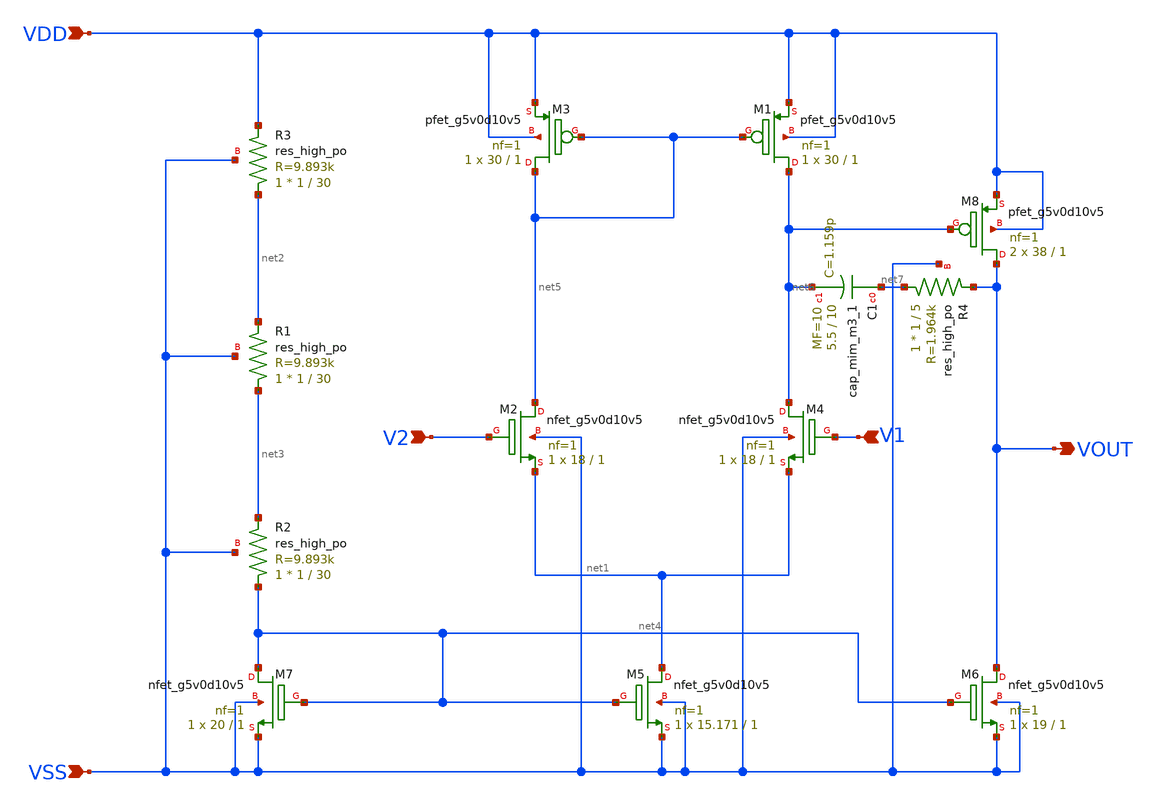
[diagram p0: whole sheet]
** sch_path: xschem/opamp.sch
**.subckt opamp VSS VDD V2 V1 VOUT
*.ipin VSS
*.ipin VDD
*.ipin V2
*.ipin V1
*.opin VOUT
XM2 net5 V2 net1 VSS sky130_fd_pr__nfet_g5v0d10v5 L=1 W=18 nf=1 ad='int((nf+1)/2) * W/nf * 0.29' as='int((nf+2)/2) * W/nf * 0.29'
+ pd='2*int((nf+1)/2) * (W/nf + 0.29)' ps='2*int((nf+2)/2) * (W/nf + 0.29)' nrd='0.29 / W' nrs='0.29 / W'
+ sa=0 sb=0 sd=0 mult=1 m=1
XM1 net6 net5 VDD VDD sky130_fd_pr__pfet_g5v0d10v5 L=1 W=30 nf=1 ad='int((nf+1)/2) * W/nf * 0.29' as='int((nf+2)/2) * W/nf * 0.29'
+ pd='2*int((nf+1)/2) * (W/nf + 0.29)' ps='2*int((nf+2)/2) * (W/nf + 0.29)' nrd='0.29 / W' nrs='0.29 / W'
+ sa=0 sb=0 sd=0 mult=1 m=1
XM4 net6 V1 net1 VSS sky130_fd_pr__nfet_g5v0d10v5 L=1 W=18 nf=1 ad='int((nf+1)/2) * W/nf * 0.29' as='int((nf+2)/2) * W/nf * 0.29'
+ pd='2*int((nf+1)/2) * (W/nf + 0.29)' ps='2*int((nf+2)/2) * (W/nf + 0.29)' nrd='0.29 / W' nrs='0.29 / W'
+ sa=0 sb=0 sd=0 mult=1 m=1
XM5 net1 net4 VSS VSS sky130_fd_pr__nfet_g5v0d10v5 L=1 W=15.171 nf=1 ad='int((nf+1)/2) * W/nf * 0.29'
+ as='int((nf+2)/2) * W/nf * 0.29' pd='2*int((nf+1)/2) * (W/nf + 0.29)' ps='2*int((nf+2)/2) * (W/nf + 0.29)'
+ nrd='0.29 / W' nrs='0.29 / W' sa=0 sb=0 sd=0 mult=1 m=1
XM6 VOUT net4 VSS VSS sky130_fd_pr__nfet_g5v0d10v5 L=1 W=19 nf=1 ad='int((nf+1)/2) * W/nf * 0.29' as='int((nf+2)/2) * W/nf * 0.29'
+ pd='2*int((nf+1)/2) * (W/nf + 0.29)' ps='2*int((nf+2)/2) * (W/nf + 0.29)' nrd='0.29 / W' nrs='0.29 / W'
+ sa=0 sb=0 sd=0 mult=1 m=1
XM7 net4 net4 VSS VSS sky130_fd_pr__nfet_g5v0d10v5 L=1 W=20 nf=1 ad='int((nf+1)/2) * W/nf * 0.29' as='int((nf+2)/2) * W/nf * 0.29'
+ pd='2*int((nf+1)/2) * (W/nf + 0.29)' ps='2*int((nf+2)/2) * (W/nf + 0.29)' nrd='0.29 / W' nrs='0.29 / W'
+ sa=0 sb=0 sd=0 mult=1 m=1
XM3 net5 net5 VDD VDD sky130_fd_pr__pfet_g5v0d10v5 L=1 W=30 nf=1 ad='int((nf+1)/2) * W/nf * 0.29' as='int((nf+2)/2) * W/nf * 0.29'
+ pd='2*int((nf+1)/2) * (W/nf + 0.29)' ps='2*int((nf+2)/2) * (W/nf + 0.29)' nrd='0.29 / W' nrs='0.29 / W'
+ sa=0 sb=0 sd=0 mult=1 m=1
XM8 VOUT net6 VDD VDD sky130_fd_pr__pfet_g5v0d10v5 L=1 W=38 nf=1 ad='int((nf+1)/2) * W/nf * 0.29' as='int((nf+2)/2) * W/nf * 0.29'
+ pd='2*int((nf+1)/2) * (W/nf + 0.29)' ps='2*int((nf+2)/2) * (W/nf + 0.29)' nrd='0.29 / W' nrs='0.29 / W'
+ sa=0 sb=0 sd=0 mult=2 m=2
XR3 net2 VDD VSS sky130_fd_pr__res_high_po W=1 L=30 mult=1 m=1
XR1 net3 net2 VSS sky130_fd_pr__res_high_po W=1 L=30 mult=1 m=1
XR2 net4 net3 VSS sky130_fd_pr__res_high_po W=1 L=30 mult=1 m=1
XR4 net7 VOUT VSS sky130_fd_pr__res_high_po W=1 L=5 mult=1 m=1
XC1 net7 net6 sky130_fd_pr__cap_mim_m3_1 W=5.5 L=10 MF=10 m=10
**.ends
.end
